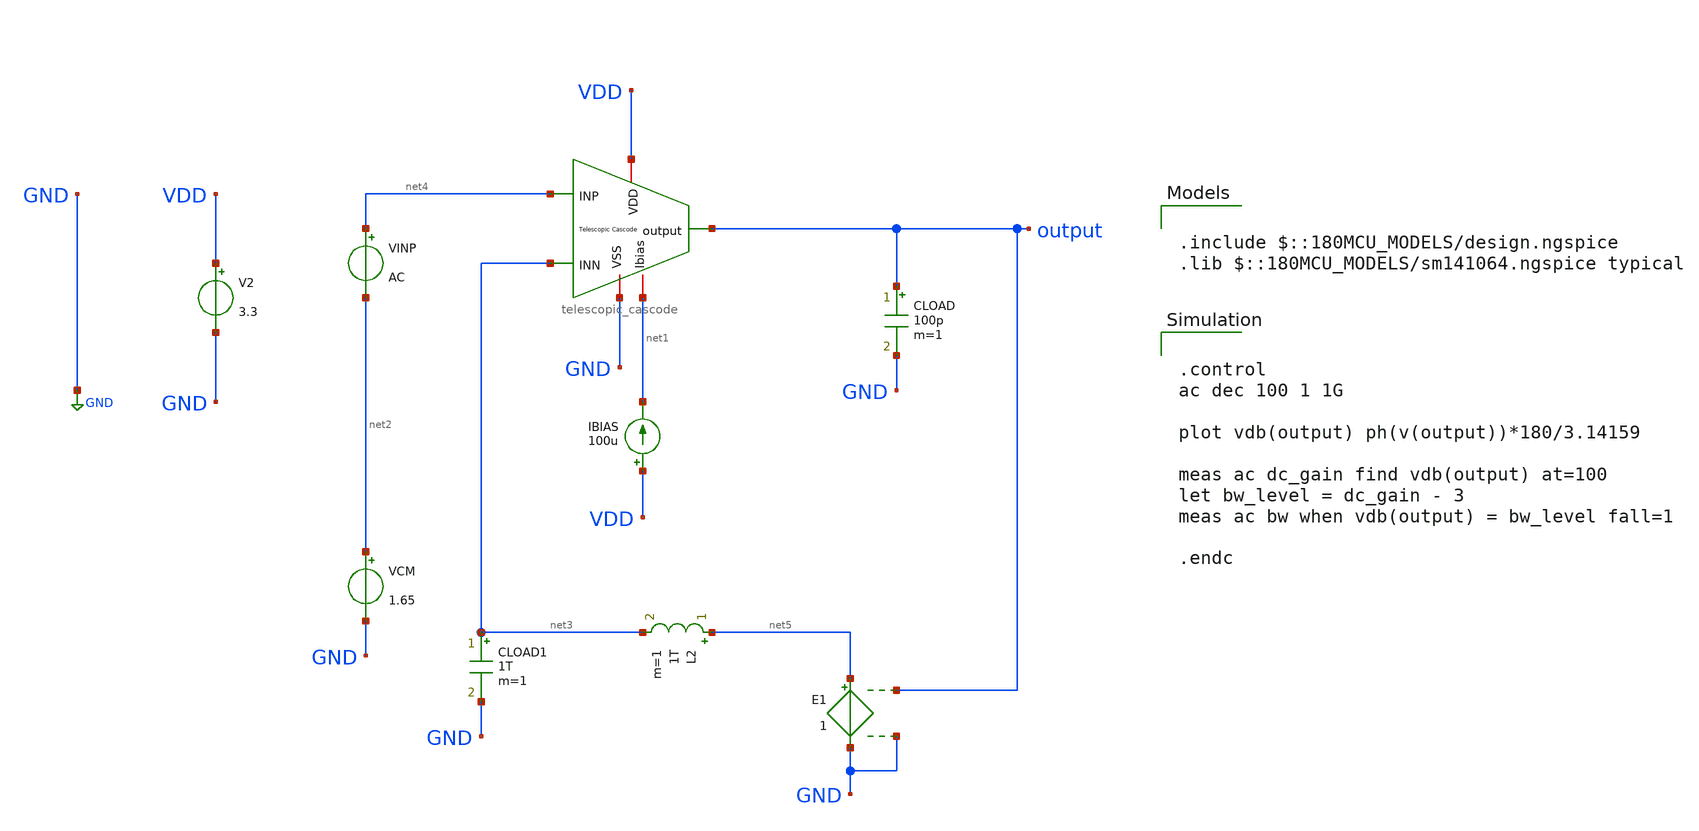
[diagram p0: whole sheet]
** sch_path: designs/libs/core_amps/ota_telescopic/tb/telescopic_ac_open_tb.sch
**.subckt telescopic_ac_open_tb
IBIAS VDD net1 100u
V2 VDD GND 3.3
CLOAD output GND 100p m=1
VINP net4 net2 AC
VCM net2 GND 1.65
L2 net5 net3 1T m=1
CLOAD1 net3 GND 1T m=1
E1 net5 GND output GND 1
x1 VDD output net3 net4 GND net1 telescopic_cascode
**** begin user architecture code

.include $::180MCU_MODELS/design.ngspice
.lib $::180MCU_MODELS/sm141064.ngspice typical



.control
ac dec 100 1 1G

plot vdb(output) ph(v(output))*180/3.14159

meas ac dc_gain find vdb(output) at=100
let bw_level = dc_gain - 3
meas ac bw when vdb(output) = bw_level fall=1

.endc



**** end user architecture code
**.ends
.GLOBAL GND
.end
